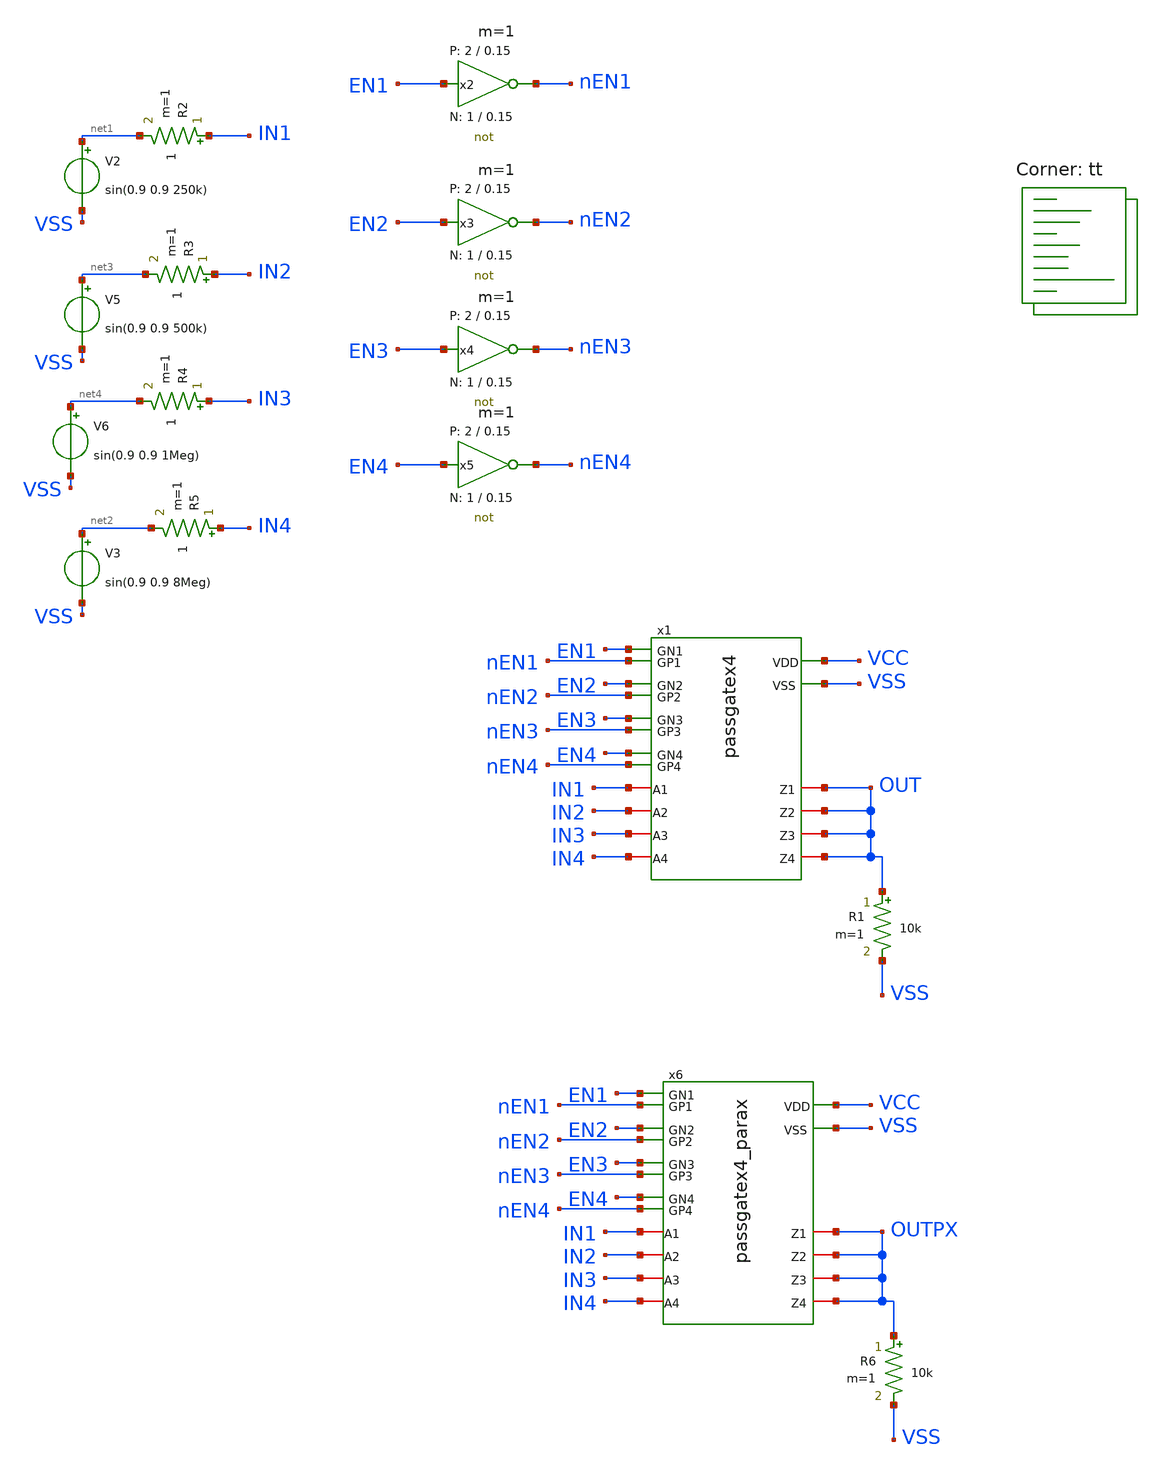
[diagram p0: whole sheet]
** sch_path: xschem/tb_passgatex4.sch
* StefanSchippers/xschem_sky130/sky130_tests/not.sch:
* Copyright 2021 Stefan Frederik Schippers
* Licensed under the Apache License, Version 2.0 (the "License");
**.subckt tb_passgatex4
x1 nEN3 nEN2 nEN1 VCC nEN4 VSS IN3 IN2 IN1 OUT OUT OUT IN4 OUT EN3 EN2 EN1 EN4 passgatex4
x2 nEN1 EN1 VCC VSS not W_N=1 L_N=0.15 W_P=2 L_P=0.15 m=1
V2 net1 VSS sin(0.9 0.9 250k)
x3 nEN2 EN2 VCC VSS not W_N=1 L_N=0.15 W_P=2 L_P=0.15 m=1
x4 nEN3 EN3 VCC VSS not W_N=1 L_N=0.15 W_P=2 L_P=0.15 m=1
x5 nEN4 EN4 VCC VSS not W_N=1 L_N=0.15 W_P=2 L_P=0.15 m=1
V3 net2 VSS sin(0.9 0.9 8Meg)
V5 net3 VSS sin(0.9 0.9 500k)
V6 net4 VSS sin(0.9 0.9 1Meg)
R1 OUT VSS 10k m=1
R2 IN1 net1 1 m=1
R3 IN2 net3 1 m=1
R4 IN3 net4 1 m=1
R5 IN4 net2 1 m=1
x6 nEN3 nEN2 nEN1 VCC nEN4 VSS IN3 IN2 IN1 OUTPX OUTPX OUTPX IN4 OUTPX EN3 EN2 EN1 EN4
+ passgatex4_parax
R6 OUTPX VSS 10k m=1
**** begin user architecture code
.lib $::SKYWATER_MODELS/sky130.lib.spice tt
**** end user architecture code
**.ends

* expanding   symbol:  /home/ttuser/work/tt09-analogmux/xschem/passgatex4.sym # of pins=18
** sym_path: xschem/passgatex4.sym
** sch_path: xschem/passgatex4.sch
.subckt passgatex4 GP3 GP2 GP1 VDD GP4 VSS A3 A2 A1 Z3 Z1 Z2 A4 Z4 GN3 GN2 GN1 GN4
*.ipin VDD
*.ipin VSS
*.ipin GP1
*.ipin GN1
*.iopin A1
*.iopin Z1
*.ipin GP2
*.ipin GN2
*.iopin A2
*.iopin Z2
*.ipin GP3
*.ipin GN3
*.iopin A3
*.iopin Z3
*.ipin GP4
*.ipin GN4
*.iopin A4
*.iopin Z4
x1 Z1 A1 GP1 GN1 VSS VDD passgate
x2 Z2 A2 GP2 GN2 VSS VDD passgate
x3 Z3 A3 GP3 GN3 VSS VDD passgate
x4 Z4 A4 GP4 GN4 VSS VDD passgate
.ends


* expanding   symbol:  sky130_tests/not.sym # of pins=2
** sym_path: sky130_tests/not.sym
** sch_path: sky130_tests/not.sch
.subckt not y a VCCPIN VSSPIN     W_N=1 L_N=0.15 W_P=2 L_P=0.15
*.opin y
*.ipin a
XM1 DN a VSSPIN VSSPIN sky130_fd_pr__nfet_01v8 L=L_N W=W_N nf=1 ad='int((1 + 1)/2) * W_N / 1 * 0.29'
+ as='int((1 + 2)/2) * W_N / 1 * 0.29' pd='2*int((1 + 1)/2) * (W_N / 1 + 0.29)' ps='2*int((1 + 2)/2) * (W_N / 1 + 0.29)'
+ nrd='0.29 / W_N ' nrs='0.29 / W_N ' sa=0 sb=0 sd=0 mult=1 m=1
XM2 DP a VCCPIN VCCPIN sky130_fd_pr__pfet_01v8 L=L_P W=W_P nf=1 ad='int((nf+1)/2) * W/nf * 0.29' as='int((nf+2)/2) * W/nf * 0.29'
+ pd='2*int((nf+1)/2) * (W/nf + 0.29)' ps='2*int((nf+2)/2) * (W/nf + 0.29)' nrd='0.29 / W' nrs='0.29 / W'
+ sa=0 sb=0 sd=0 mult=1 m=1
Vmeas DP y 0
.save i(vmeas)
Vmeas1 y DN 0
.save i(vmeas1)
.save v(dp)
.save v(dn)
.ends


* expanding   symbol:  /home/ttuser/work/tt09-analogmux/xschem/passgatex4_parax.sym # of pins=18
** sym_path: xschem/passgatex4.sym
.include [file normalize extracted/passgatex4_parax.spice]

* expanding   symbol:  /home/ttuser/tt08-wowa2/xschem/passgate.sym # of pins=6
** sym_path: xschem/passgate.sym
** sch_path: xschem/passgate.sch
.subckt passgate Z A GP GN VSSBPIN VCCBPIN
*.ipin GN
*.ipin VCCBPIN
*.ipin VSSBPIN
*.ipin GP
*.iopin A
*.iopin Z
XM1 Z GN A VSSBPIN sky130_fd_pr__nfet_01v8_lvt L=0.35 W=8 nf=1 ad='int((nf+1)/2) * W/nf * 0.29' as='int((nf+2)/2) * W/nf * 0.29'
+ pd='2*int((nf+1)/2) * (W/nf + 0.29)' ps='2*int((nf+2)/2) * (W/nf + 0.29)' nrd='0.29 / W' nrs='0.29 / W'
+ sa=0 sb=0 sd=0 mult=2 m=2
XM3 Z GP A VCCBPIN sky130_fd_pr__pfet_01v8_lvt L=0.35 W=10 nf=1 ad='int((nf+1)/2) * W/nf * 0.29' as='int((nf+2)/2) * W/nf * 0.29'
+ pd='2*int((nf+1)/2) * (W/nf + 0.29)' ps='2*int((nf+2)/2) * (W/nf + 0.29)' nrd='0.29 / W' nrs='0.29 / W'
+ sa=0 sb=0 sd=0 mult=2 m=2
.ends

**** begin user architecture code


* ngspice commands
* .options savecurrents
.param VCC = 1.8
.param SRCRES = 1k
.include stimuli_tb_passgatex4.cir
.control
save all
op
write tb_passgatex4.raw
set appendwrite
tran 10n 50u
write tb_passgatex4.raw
quit 0
.endc



**** end user architecture code
.end
